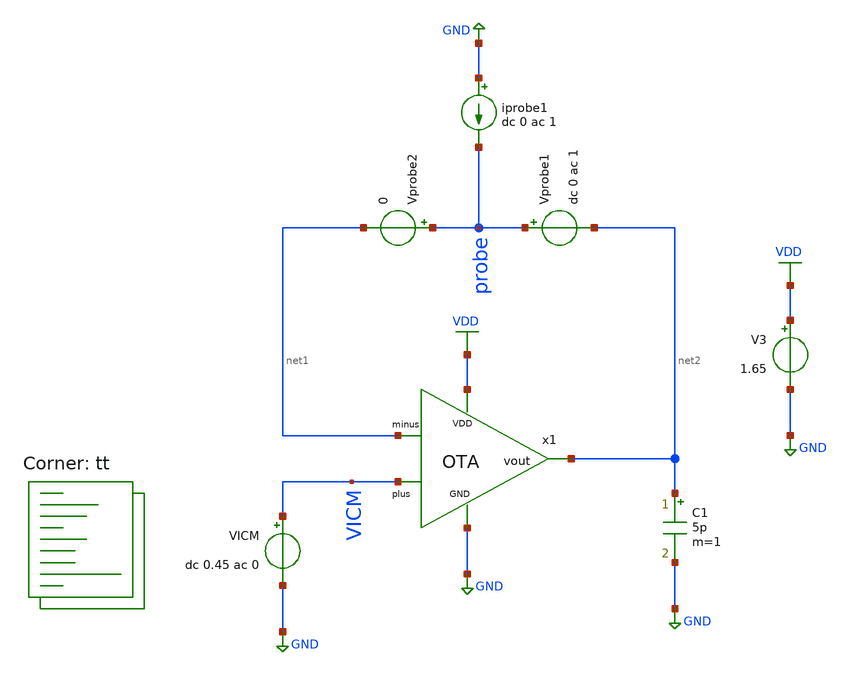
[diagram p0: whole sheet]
** sch_path: Schematic/OTA/OTA_STB_TB_.sch
**.subckt OTA_STB_TB_
x1 VDD net1 VICM net2 GND OTA
Vprobe2 probe net1 0
Vprobe1 probe net2 dc 0 ac 1
iprobe1 GND probe dc 0 ac 1
VICM VICM GND dc 0.45 ac 0
C1 net2 GND 5p m=1
V3 VDD GND 1.65
**** begin user architecture code


.options savecurrents
.control
 let runs=2
 let run=0

 alter @Vprobe1[acmag]=1
 alter @iprobe1[acmag]=0

 dowhile run < runs

 set run =”$&run”
 ac dec 20 0.01 10G
 write OTA_STB_TB_{$run}.raw

 all
 alter @Vprobe1[acmag]=0
 alter @iprobe1[acmag]=1
 let run = run + 1
 end

 let ip22 = ac2.i(Vprobe2)
 let vprb1 = ac1.probe
 let mb = 1/(vprb1+ip22)-1
 let phase_mb = 180/PI*vp(mb)
 plot vdb(mb)
 plot phase_mb
 plot vdb(mb) phase_mb
 write OTA-tt.txt vdb(mb)

 meas ac peak MAX vmag(mb) FROM=2 TO=1.5G
 let f3db = peak/sqrt(2)
 meas ac f1 WHEN vmag(mb)=f3db RISE=1
 meas ac BW WHEN vmag(mb)=f3db FALL=1
 let GBW = peak*BW
 meas ac pm_deg find phase_mb when vdb(mb)=0
 meas ac dominant_pole_f when vdb(mb)=0
 meas ac loop_gain find vdb(mb) at=0.01
 print GBW

 op
 show m : gm : gmbs : gds : vds : vdsat : vgs : vth : id
.endc

.lib $::SKYWATER_MODELS/sky130.lib.spice tt
**** end user architecture code
**.ends
.GLOBAL VDD
.GLOBAL GND
.end
